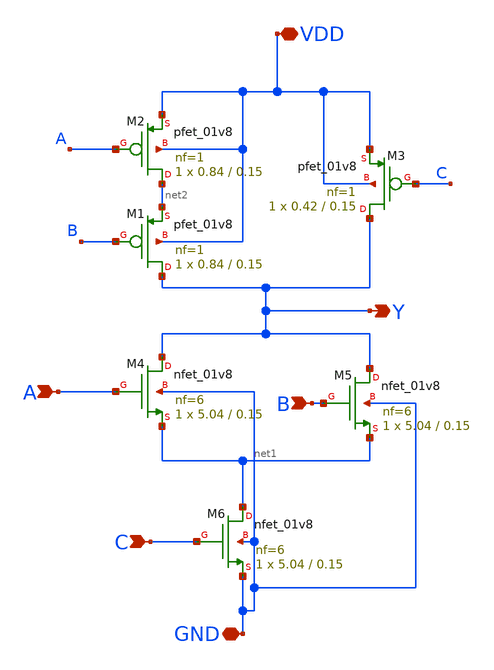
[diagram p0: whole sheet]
** sch_path: cells/OAI3X1/schematic/oai3x1.sch
**.subckt oai3x1 VDD GND A B C Y
*.iopin VDD
*.iopin GND
*.ipin A
*.ipin B
*.ipin C
*.opin Y
XM2 net2 A VDD VDD sky130_fd_pr__pfet_01v8 L=0.15 W=0.84 nf=1 ad='int((1 + 1)/2) * 0.84 / 1 * 0.29' as='int((1 + 2)/2) * 0.84 / 1 * 0.29'
+ pd='2*int((1 + 1)/2) * (0.84 / 1 + 0.29)' ps='2*int((1 + 2)/2) * (0.84 / 1 + 0.29)' nrd='0.29 / 0.84 '
+ nrs='0.29 / 0.84 ' sa=0 sb=0 sd=0 mult=1 m=1
XM3 Y C VDD VDD sky130_fd_pr__pfet_01v8 L=0.15 W=0.42 nf=1 ad='int((1 + 1)/2) * 0.42 / 1 * 0.29' as='int((1 + 2)/2) * 0.42 / 1 * 0.29'
+ pd='2*int((1 + 1)/2) * (0.42 / 1 + 0.29)' ps='2*int((1 + 2)/2) * (0.42 / 1 + 0.29)' nrd='0.29 / 0.42 '
+ nrs='0.29 / 0.42 ' sa=0 sb=0 sd=0 mult=1 m=1
XM4 Y A net1 GND sky130_fd_pr__nfet_01v8 L=0.15 W=5.04 nf=6 ad='int((6 + 1)/2) * 5.04 / 6 * 0.29' as='int((6 + 2)/2) * 5.04 / 6 * 0.29'
+ pd='2*int((6 + 1)/2) * (5.04 / 6 + 0.29)' ps='2*int((6 + 2)/2) * (5.04 / 6 + 0.29)' nrd='0.29 / 5.04 '
+ nrs='0.29 / 5.04 ' sa=0 sb=0 sd=0 mult=1 m=1
XM1 Y B net2 VDD sky130_fd_pr__pfet_01v8 L=0.15 W=0.84 nf=1 ad='int((1 + 1)/2) * 0.84 / 1 * 0.29' as='int((1 + 2)/2) * 0.84 / 1 * 0.29'
+ pd='2*int((1 + 1)/2) * (0.84 / 1 + 0.29)' ps='2*int((1 + 2)/2) * (0.84 / 1 + 0.29)' nrd='0.29 / 0.84 '
+ nrs='0.29 / 0.84 ' sa=0 sb=0 sd=0 mult=1 m=1
XM6 net1 C GND GND sky130_fd_pr__nfet_01v8 L=0.15 W=5.04 nf=6 ad='int((6 + 1)/2) * 5.04 / 6 * 0.29' as='int((6 + 2)/2) * 5.04 / 6 * 0.29'
+ pd='2*int((6 + 1)/2) * (5.04 / 6 + 0.29)' ps='2*int((6 + 2)/2) * (5.04 / 6 + 0.29)' nrd='0.29 / 5.04 '
+ nrs='0.29 / 5.04 ' sa=0 sb=0 sd=0 mult=1 m=1
XM5 Y B net1 GND sky130_fd_pr__nfet_01v8 L=0.15 W=5.04 nf=6 ad='int((6 + 1)/2) * 5.04 / 6 * 0.29' as='int((6 + 2)/2) * 5.04 / 6 * 0.29'
+ pd='2*int((6 + 1)/2) * (5.04 / 6 + 0.29)' ps='2*int((6 + 2)/2) * (5.04 / 6 + 0.29)' nrd='0.29 / 5.04 '
+ nrs='0.29 / 5.04 ' sa=0 sb=0 sd=0 mult=1 m=1
**.ends
.end
